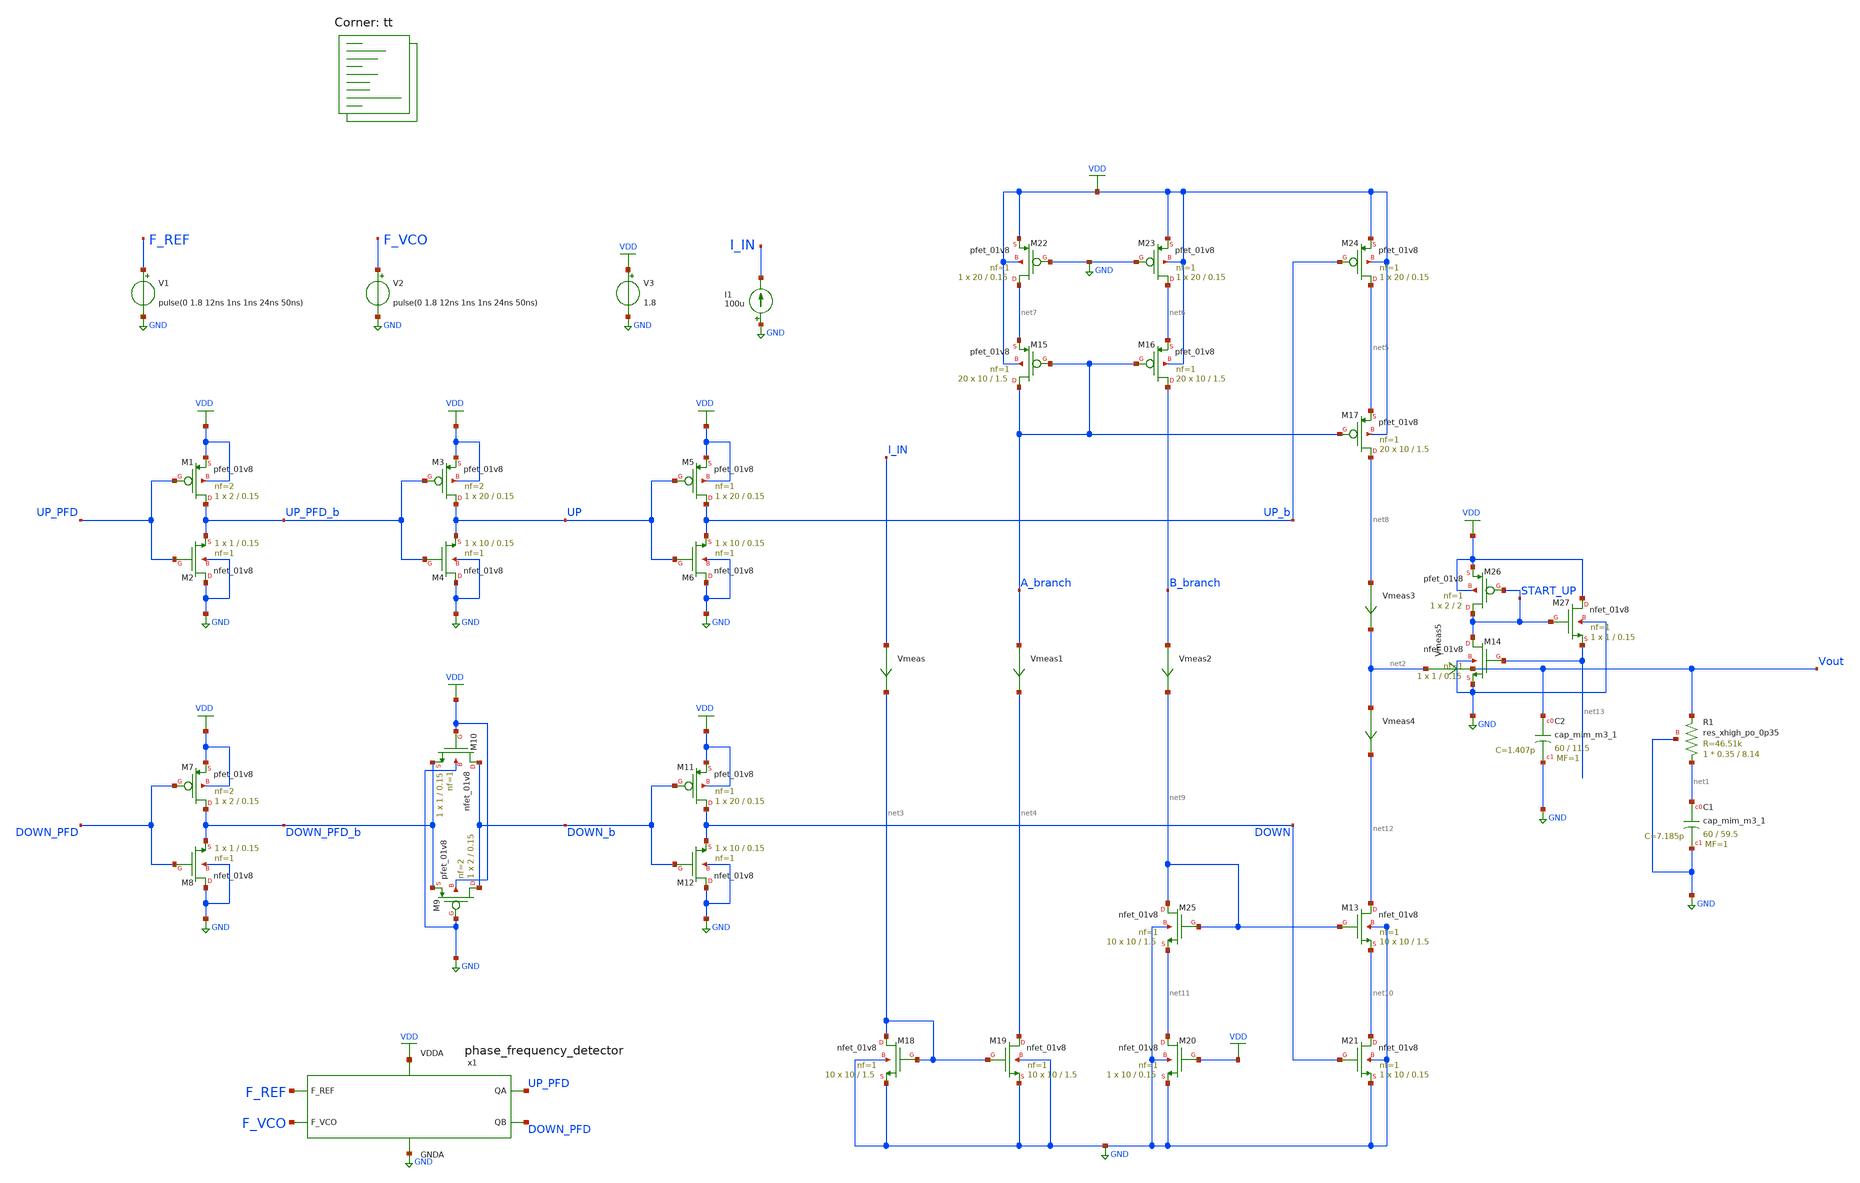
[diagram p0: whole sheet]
** sch_path: projects/pll/charge_pump/xschem_ngspice/pfd_charge_pump_11.sch
**.subckt pfd_charge_pump_11
V3 VDD GND 1.8
XC2 Vout GND sky130_fd_pr__cap_mim_m3_1 W=60 L=11.5 MF=1 m=1
XC1 net1 GND sky130_fd_pr__cap_mim_m3_1 W=60 L=59.5 MF=1 m=1
V1 F_REF GND pulse(0 1.8 12ns 1ns 1ns 24ns 50ns)
V2 F_VCO GND pulse(0 1.8 12ns 1ns 1ns 24ns 50ns)
x1 F_REF F_VCO VDD UP_PFD DOWN_PFD GND phase_frequency_detector
XR1 net1 Vout GND sky130_fd_pr__res_xhigh_po_0p35 L=8.14 mult=1 m=1
I1 GND I_IN 100u
Vmeas5 net2 Vout 0
.save i(vmeas5)
XM18 net3 net3 GND GND sky130_fd_pr__nfet_01v8 L=1.5 W=10 nf=1 ad='int((nf+1)/2) * W/nf * 0.29' as='int((nf+2)/2) * W/nf * 0.29'
+ pd='2*int((nf+1)/2) * (W/nf + 0.29)' ps='2*int((nf+2)/2) * (W/nf + 0.29)' nrd='0.29 / W' nrs='0.29 / W'
+ sa=0 sb=0 sd=0 mult=10 m=10
XM19 net4 net3 GND GND sky130_fd_pr__nfet_01v8 L=1.5 W=10 nf=1 ad='int((nf+1)/2) * W/nf * 0.29' as='int((nf+2)/2) * W/nf * 0.29'
+ pd='2*int((nf+1)/2) * (W/nf + 0.29)' ps='2*int((nf+2)/2) * (W/nf + 0.29)' nrd='0.29 / W' nrs='0.29 / W'
+ sa=0 sb=0 sd=0 mult=10 m=10
Vmeas I_IN net3 0
.save i(vmeas)
Vmeas3 net8 net2 0
.save i(vmeas3)
Vmeas4 net2 net12 0
.save i(vmeas4)
XM17 net8 A_branch net5 VDD sky130_fd_pr__pfet_01v8 L=1.5 W=10 nf=1 ad='int((nf+1)/2) * W/nf * 0.29'
+ as='int((nf+2)/2) * W/nf * 0.29' pd='2*int((nf+1)/2) * (W/nf + 0.29)' ps='2*int((nf+2)/2) * (W/nf + 0.29)'
+ nrd='0.29 / W' nrs='0.29 / W' sa=0 sb=0 sd=0 mult=20 m=20
XM21 net10 DOWN GND GND sky130_fd_pr__nfet_01v8 L=0.15 W=10 nf=1 ad='int((nf+1)/2) * W/nf * 0.29' as='int((nf+2)/2) * W/nf * 0.29'
+ pd='2*int((nf+1)/2) * (W/nf + 0.29)' ps='2*int((nf+2)/2) * (W/nf + 0.29)' nrd='0.29 / W' nrs='0.29 / W'
+ sa=0 sb=0 sd=0 mult=1 m=1
XM20 net11 VDD GND GND sky130_fd_pr__nfet_01v8 L=0.15 W=10 nf=1 ad='int((nf+1)/2) * W/nf * 0.29' as='int((nf+2)/2) * W/nf * 0.29'
+ pd='2*int((nf+1)/2) * (W/nf + 0.29)' ps='2*int((nf+2)/2) * (W/nf + 0.29)' nrd='0.29 / W' nrs='0.29 / W'
+ sa=0 sb=0 sd=0 mult=1 m=1
XM15 A_branch A_branch net7 VDD sky130_fd_pr__pfet_01v8 L=1.5 W=10 nf=1 ad='int((nf+1)/2) * W/nf * 0.29'
+ as='int((nf+2)/2) * W/nf * 0.29' pd='2*int((nf+1)/2) * (W/nf + 0.29)' ps='2*int((nf+2)/2) * (W/nf + 0.29)'
+ nrd='0.29 / W' nrs='0.29 / W' sa=0 sb=0 sd=0 mult=20 m=20
XM16 B_branch A_branch net6 VDD sky130_fd_pr__pfet_01v8 L=1.5 W=10 nf=1 ad='int((nf+1)/2) * W/nf * 0.29'
+ as='int((nf+2)/2) * W/nf * 0.29' pd='2*int((nf+1)/2) * (W/nf + 0.29)' ps='2*int((nf+2)/2) * (W/nf + 0.29)'
+ nrd='0.29 / W' nrs='0.29 / W' sa=0 sb=0 sd=0 mult=20 m=20
Vmeas1 A_branch net4 0
.save i(vmeas1)
Vmeas2 B_branch net9 0
.save i(vmeas2)
XM9 DOWN_b GND DOWN_PFD_b VDD sky130_fd_pr__pfet_01v8 L=0.15 W=2 nf=2 ad='int((nf+1)/2) * W/nf * 0.29'
+ as='int((nf+2)/2) * W/nf * 0.29' pd='2*int((nf+1)/2) * (W/nf + 0.29)' ps='2*int((nf+2)/2) * (W/nf + 0.29)'
+ nrd='0.29 / W' nrs='0.29 / W' sa=0 sb=0 sd=0 mult=1 m=1
XM10 DOWN_b VDD DOWN_PFD_b GND sky130_fd_pr__nfet_01v8 L=0.15 W=1 nf=1 ad='int((nf+1)/2) * W/nf * 0.29'
+ as='int((nf+2)/2) * W/nf * 0.29' pd='2*int((nf+1)/2) * (W/nf + 0.29)' ps='2*int((nf+2)/2) * (W/nf + 0.29)'
+ nrd='0.29 / W' nrs='0.29 / W' sa=0 sb=0 sd=0 mult=1 m=1
XM1 UP_PFD_b UP_PFD VDD VDD sky130_fd_pr__pfet_01v8 L=0.15 W=2 nf=2 ad='int((nf+1)/2) * W/nf * 0.29'
+ as='int((nf+2)/2) * W/nf * 0.29' pd='2*int((nf+1)/2) * (W/nf + 0.29)' ps='2*int((nf+2)/2) * (W/nf + 0.29)'
+ nrd='0.29 / W' nrs='0.29 / W' sa=0 sb=0 sd=0 mult=1 m=1
XM2 GND UP_PFD UP_PFD_b GND sky130_fd_pr__nfet_01v8 L=0.15 W=1 nf=1 ad='int((nf+1)/2) * W/nf * 0.29'
+ as='int((nf+2)/2) * W/nf * 0.29' pd='2*int((nf+1)/2) * (W/nf + 0.29)' ps='2*int((nf+2)/2) * (W/nf + 0.29)'
+ nrd='0.29 / W' nrs='0.29 / W' sa=0 sb=0 sd=0 mult=1 m=1
XM7 DOWN_PFD_b DOWN_PFD VDD VDD sky130_fd_pr__pfet_01v8 L=0.15 W=2 nf=2 ad='int((nf+1)/2) * W/nf * 0.29'
+ as='int((nf+2)/2) * W/nf * 0.29' pd='2*int((nf+1)/2) * (W/nf + 0.29)' ps='2*int((nf+2)/2) * (W/nf + 0.29)'
+ nrd='0.29 / W' nrs='0.29 / W' sa=0 sb=0 sd=0 mult=1 m=1
XM8 GND DOWN_PFD DOWN_PFD_b GND sky130_fd_pr__nfet_01v8 L=0.15 W=1 nf=1 ad='int((nf+1)/2) * W/nf * 0.29'
+ as='int((nf+2)/2) * W/nf * 0.29' pd='2*int((nf+1)/2) * (W/nf + 0.29)' ps='2*int((nf+2)/2) * (W/nf + 0.29)'
+ nrd='0.29 / W' nrs='0.29 / W' sa=0 sb=0 sd=0 mult=1 m=1
XM3 UP UP_PFD_b VDD VDD sky130_fd_pr__pfet_01v8 L=0.15 W=20 nf=2 ad='int((nf+1)/2) * W/nf * 0.29' as='int((nf+2)/2) * W/nf * 0.29'
+ pd='2*int((nf+1)/2) * (W/nf + 0.29)' ps='2*int((nf+2)/2) * (W/nf + 0.29)' nrd='0.29 / W' nrs='0.29 / W'
+ sa=0 sb=0 sd=0 mult=1 m=1
XM4 GND UP_PFD_b UP GND sky130_fd_pr__nfet_01v8 L=0.15 W=10 nf=1 ad='int((nf+1)/2) * W/nf * 0.29' as='int((nf+2)/2) * W/nf * 0.29'
+ pd='2*int((nf+1)/2) * (W/nf + 0.29)' ps='2*int((nf+2)/2) * (W/nf + 0.29)' nrd='0.29 / W' nrs='0.29 / W'
+ sa=0 sb=0 sd=0 mult=1 m=1
XM5 UP_b UP VDD VDD sky130_fd_pr__pfet_01v8 L=0.15 W=20 nf=1 ad='int((nf+1)/2) * W/nf * 0.29' as='int((nf+2)/2) * W/nf * 0.29'
+ pd='2*int((nf+1)/2) * (W/nf + 0.29)' ps='2*int((nf+2)/2) * (W/nf + 0.29)' nrd='0.29 / W' nrs='0.29 / W'
+ sa=0 sb=0 sd=0 mult=1 m=1
XM6 GND UP UP_b GND sky130_fd_pr__nfet_01v8 L=0.15 W=10 nf=1 ad='int((nf+1)/2) * W/nf * 0.29' as='int((nf+2)/2) * W/nf * 0.29'
+ pd='2*int((nf+1)/2) * (W/nf + 0.29)' ps='2*int((nf+2)/2) * (W/nf + 0.29)' nrd='0.29 / W' nrs='0.29 / W'
+ sa=0 sb=0 sd=0 mult=1 m=1
XM11 DOWN DOWN_b VDD VDD sky130_fd_pr__pfet_01v8 L=0.15 W=20 nf=1 ad='int((nf+1)/2) * W/nf * 0.29' as='int((nf+2)/2) * W/nf * 0.29'
+ pd='2*int((nf+1)/2) * (W/nf + 0.29)' ps='2*int((nf+2)/2) * (W/nf + 0.29)' nrd='0.29 / W' nrs='0.29 / W'
+ sa=0 sb=0 sd=0 mult=1 m=1
XM12 GND DOWN_b DOWN GND sky130_fd_pr__nfet_01v8 L=0.15 W=10 nf=1 ad='int((nf+1)/2) * W/nf * 0.29' as='int((nf+2)/2) * W/nf * 0.29'
+ pd='2*int((nf+1)/2) * (W/nf + 0.29)' ps='2*int((nf+2)/2) * (W/nf + 0.29)' nrd='0.29 / W' nrs='0.29 / W'
+ sa=0 sb=0 sd=0 mult=1 m=1
XM22 net7 GND VDD VDD sky130_fd_pr__pfet_01v8 L=0.15 W=20 nf=1 ad='int((nf+1)/2) * W/nf * 0.29' as='int((nf+2)/2) * W/nf * 0.29'
+ pd='2*int((nf+1)/2) * (W/nf + 0.29)' ps='2*int((nf+2)/2) * (W/nf + 0.29)' nrd='0.29 / W' nrs='0.29 / W'
+ sa=0 sb=0 sd=0 mult=1 m=1
XM23 net6 GND VDD VDD sky130_fd_pr__pfet_01v8 L=0.15 W=20 nf=1 ad='int((nf+1)/2) * W/nf * 0.29' as='int((nf+2)/2) * W/nf * 0.29'
+ pd='2*int((nf+1)/2) * (W/nf + 0.29)' ps='2*int((nf+2)/2) * (W/nf + 0.29)' nrd='0.29 / W' nrs='0.29 / W'
+ sa=0 sb=0 sd=0 mult=1 m=1
XM24 net5 UP_b VDD VDD sky130_fd_pr__pfet_01v8 L=0.15 W=20 nf=1 ad='int((nf+1)/2) * W/nf * 0.29' as='int((nf+2)/2) * W/nf * 0.29'
+ pd='2*int((nf+1)/2) * (W/nf + 0.29)' ps='2*int((nf+2)/2) * (W/nf + 0.29)' nrd='0.29 / W' nrs='0.29 / W'
+ sa=0 sb=0 sd=0 mult=1 m=1
XM13 net12 net9 net10 GND sky130_fd_pr__nfet_01v8 L=1.5 W=10 nf=1 ad='int((nf+1)/2) * W/nf * 0.29' as='int((nf+2)/2) * W/nf * 0.29'
+ pd='2*int((nf+1)/2) * (W/nf + 0.29)' ps='2*int((nf+2)/2) * (W/nf + 0.29)' nrd='0.29 / W' nrs='0.29 / W'
+ sa=0 sb=0 sd=0 mult=10 m=10
XM25 net9 net9 net11 GND sky130_fd_pr__nfet_01v8 L=1.5 W=10 nf=1 ad='int((nf+1)/2) * W/nf * 0.29' as='int((nf+2)/2) * W/nf * 0.29'
+ pd='2*int((nf+1)/2) * (W/nf + 0.29)' ps='2*int((nf+2)/2) * (W/nf + 0.29)' nrd='0.29 / W' nrs='0.29 / W'
+ sa=0 sb=0 sd=0 mult=10 m=10
XM14 START_UP net13 GND GND sky130_fd_pr__nfet_01v8 L=0.15 W=1 nf=1 ad='int((nf+1)/2) * W/nf * 0.29'
+ as='int((nf+2)/2) * W/nf * 0.29' pd='2*int((nf+1)/2) * (W/nf + 0.29)' ps='2*int((nf+2)/2) * (W/nf + 0.29)'
+ nrd='0.29 / W' nrs='0.29 / W' sa=0 sb=0 sd=0 mult=1 m=1
XM26 START_UP START_UP VDD VDD sky130_fd_pr__pfet_01v8 L=2 W=2 nf=1 ad='int((nf+1)/2) * W/nf * 0.29'
+ as='int((nf+2)/2) * W/nf * 0.29' pd='2*int((nf+1)/2) * (W/nf + 0.29)' ps='2*int((nf+2)/2) * (W/nf + 0.29)'
+ nrd='0.29 / W' nrs='0.29 / W' sa=0 sb=0 sd=0 mult=1 m=1
XM27 VDD START_UP net13 GND sky130_fd_pr__nfet_01v8 L=0.15 W=1 nf=1 ad='int((nf+1)/2) * W/nf * 0.29'
+ as='int((nf+2)/2) * W/nf * 0.29' pd='2*int((nf+1)/2) * (W/nf + 0.29)' ps='2*int((nf+2)/2) * (W/nf + 0.29)'
+ nrd='0.29 / W' nrs='0.29 / W' sa=0 sb=0 sd=0 mult=1 m=1
**** begin user architecture code
.lib $::SKYWATER_MODELS/sky130.lib.spice tt



.include /foss/pdks/sky130A/libs.ref/sky130_fd_sc_hd/spice/sky130_fd_sc_hd.spice

.option method=gear
.option wnflag=1
.option savecurrents

* V_out initial voltage value for the F_VCO delay of 22ns (lagging)
* .ic v(vout) = 0

* V_out initial voltage value for the F_VCO delay of 2ns  (leading)
.ic v(vout) = 1.8

* V_out initial voltage value for the F_VCO delay of 12ns (lock condition)
.ic v(vout) = 1.0

.control
  save v(f_ref) save v(f_vco) save v(up_pfd) v(down_pfd) v(up_pfd_b) v(down_pfd_b) v(up) v(up_b)
+ v(down) v(down_b) v(a_branch) v(b_branch) v(vout)

  * timestep for exact simulation results
  * tran 5ps 0.5us

  * timestep for faster simulation results
  tran 50ps 0.5us

  remzerovec
  write pfd_charge_pump_11.raw
  set appendwrite
.endc



**** end user architecture code
**.ends

* expanding   symbol:
*+  /foss/designs/my_design/projects/pll/pfd/xschem_ngspice/phase_frequency_detector.sym # of pins=6
** sym_path: projects/pll/pfd/xschem_ngspice/phase_frequency_detector.sym
** sch_path: projects/pll/pfd/xschem_ngspice/phase_frequency_detector.sch
.subckt phase_frequency_detector F_REF F_VCO VDDA QA QB GNDA
*.ipin F_REF
*.opin QA
*.ipin F_VCO
*.opin QB
*.ipin VDDA
*.ipin GNDA
x1 F_REF QA GNDA GNDA VDDA VDDA QA_b sky130_fd_sc_hd__nor2_1
x2 QA_b E GNDA GNDA VDDA VDDA QA sky130_fd_sc_hd__nor2_1
x3 QA_b E_b GNDA GNDA VDDA VDDA E sky130_fd_sc_hd__nor2_1
x4 E Reset GNDA GNDA VDDA VDDA E_b sky130_fd_sc_hd__nor2_1
x5 F_VCO QB GNDA GNDA VDDA VDDA QB_b sky130_fd_sc_hd__nor2_1
x6 QB_b F GNDA GNDA VDDA VDDA QB sky130_fd_sc_hd__nor2_1
x7 QB_b F_b GNDA GNDA VDDA VDDA F sky130_fd_sc_hd__nor2_1
x8 F Reset GNDA GNDA VDDA VDDA F_b sky130_fd_sc_hd__nor2_1
x9 QA QB GNDA GNDA VDDA VDDA before_Reset sky130_fd_sc_hd__nand2_1
x10 before_Reset GNDA GNDA VDDA VDDA net1 sky130_fd_sc_hd__inv_1
x11 net1 GNDA GNDA VDDA VDDA net2 sky130_fd_sc_hd__inv_1
x12 net2 GNDA GNDA VDDA VDDA net3 sky130_fd_sc_hd__inv_1
x13 net3 GNDA GNDA VDDA VDDA net4 sky130_fd_sc_hd__inv_1
x14 net4 GNDA GNDA VDDA VDDA Reset sky130_fd_sc_hd__inv_1
.ends

.GLOBAL GND
.GLOBAL VDD
.end
